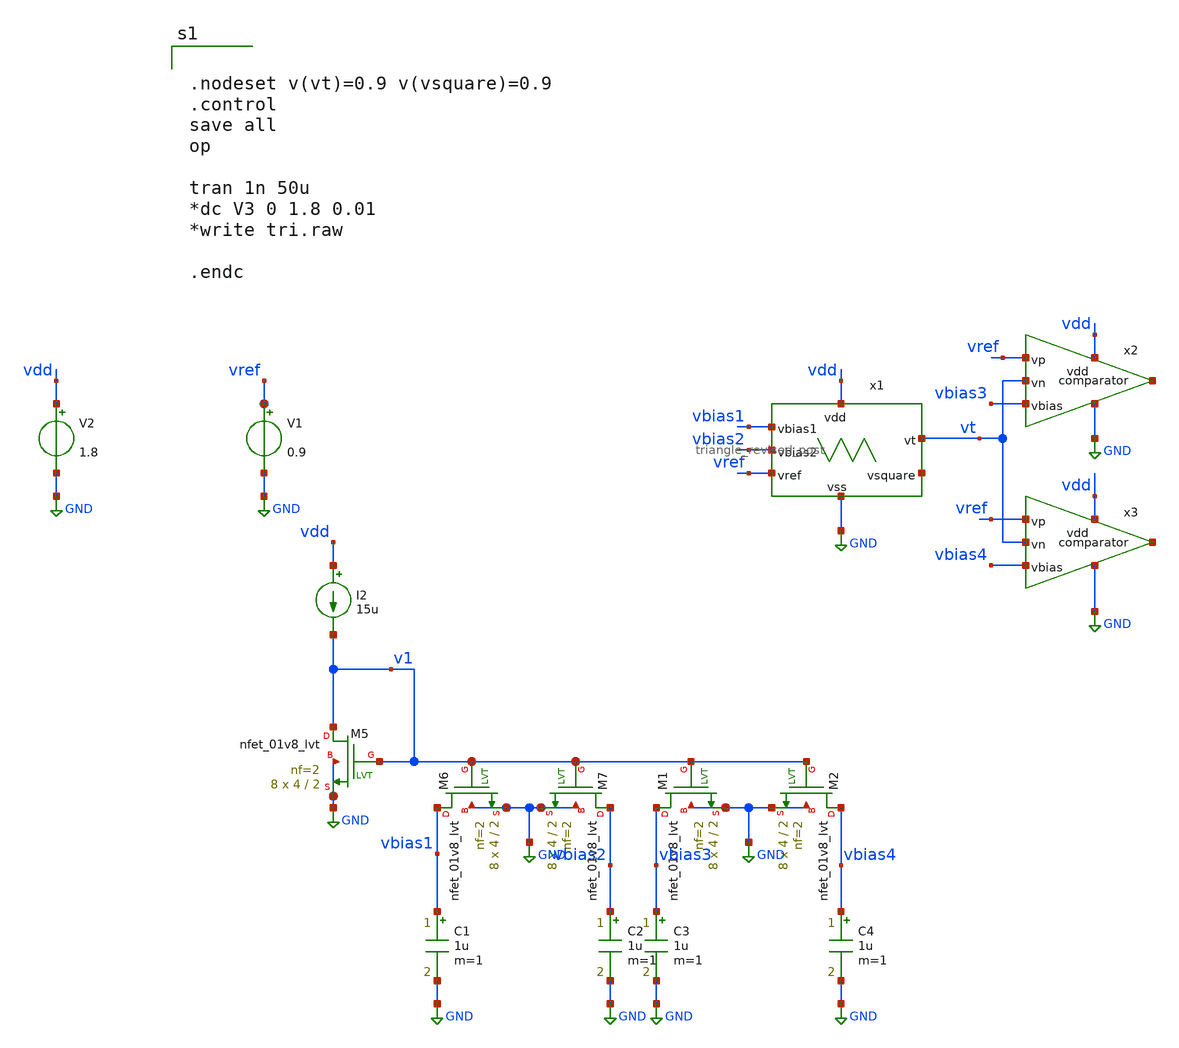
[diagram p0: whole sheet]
** sch_path: xschem/src/triangle/triangle_tb.sch
**.subckt triangle_tb
V1 vref GND 0.9
V2 vdd GND 1.8
I2 vdd v1 15u
XM5 v1 v1 GND GND sky130_fd_pr__nfet_01v8_lvt L=2 W=4 nf=2 ad='int((nf+1)/2) * W/nf * 0.29' as='int((nf+2)/2) * W/nf * 0.29'
+ pd='2*int((nf+1)/2) * (W/nf + 0.29)' ps='2*int((nf+2)/2) * (W/nf + 0.29)' nrd='0.29 / W' nrs='0.29 / W'
+ sa=0 sb=0 sd=0 mult=8 m=8
XM6 vbias1 v1 GND GND sky130_fd_pr__nfet_01v8_lvt L=2 W=4 nf=2 ad='int((nf+1)/2) * W/nf * 0.29' as='int((nf+2)/2) * W/nf * 0.29'
+ pd='2*int((nf+1)/2) * (W/nf + 0.29)' ps='2*int((nf+2)/2) * (W/nf + 0.29)' nrd='0.29 / W' nrs='0.29 / W'
+ sa=0 sb=0 sd=0 mult=8 m=8
XM7 vbias2 v1 GND GND sky130_fd_pr__nfet_01v8_lvt L=2 W=4 nf=2 ad='int((nf+1)/2) * W/nf * 0.29' as='int((nf+2)/2) * W/nf * 0.29'
+ pd='2*int((nf+1)/2) * (W/nf + 0.29)' ps='2*int((nf+2)/2) * (W/nf + 0.29)' nrd='0.29 / W' nrs='0.29 / W'
+ sa=0 sb=0 sd=0 mult=8 m=8
XM1 vbias3 v1 GND GND sky130_fd_pr__nfet_01v8_lvt L=2 W=4 nf=2 ad='int((nf+1)/2) * W/nf * 0.29' as='int((nf+2)/2) * W/nf * 0.29'
+ pd='2*int((nf+1)/2) * (W/nf + 0.29)' ps='2*int((nf+2)/2) * (W/nf + 0.29)' nrd='0.29 / W' nrs='0.29 / W'
+ sa=0 sb=0 sd=0 mult=8 m=8
XM2 vbias4 v1 GND GND sky130_fd_pr__nfet_01v8_lvt L=2 W=4 nf=2 ad='int((nf+1)/2) * W/nf * 0.29' as='int((nf+2)/2) * W/nf * 0.29'
+ pd='2*int((nf+1)/2) * (W/nf + 0.29)' ps='2*int((nf+2)/2) * (W/nf + 0.29)' nrd='0.29 / W' nrs='0.29 / W'
+ sa=0 sb=0 sd=0 mult=8 m=8
C1 vbias1 GND 1u m=1
C2 vbias2 GND 1u m=1
C3 vbias3 GND 1u m=1
C4 vbias4 GND 1u m=1
x2 vdd vref vt vbias3 GND net1 comparator
x3 vdd vref vt vbias4 GND net2 comparator
x1 vdd vbias1 vbias2 vref GND net3 vt triangle_revised_post
**** begin user architecture code

.include /home/eda/pdk/skywater-pdk/libraries/sky130_fd_pr_ngspice/latest/models/corners/tt.spice
.include /home/eda/magic/class_d_audio_amplifier/OTA/OTA_tri_post.spice
.include /home/eda/magic/class_d_audio_amplifier/OTA/OTA_post.spice
.include /home/eda/magic/class_d_audio_amplifier/triang/triangle_post.spice
.include /home/eda/magic/class_d_audio_amplifier/OTA/OTA_int_revised_post.spice
.include /home/eda/magic/class_d_audio_amplifier/OTA/OTA_revised_post.spice
.include /home/eda/magic/class_d_audio_amplifier/OTA/OTA_tri_revised_post.spice
.include /home/eda/magic/class_d_audio_amplifier/triang/triangle_revised_post.spice
* Resistor$::SKYWATER_MODELS/Capacitor
.include $::SKYWATER_MODELS/models/r+c/res_typical__cap_typical.spice
.include $::SKYWATER_MODELS/models/r+c/res_typical__cap_typical__lin.spice
* Special cells
.include $::SKYWATER_MODELS/models/corners/tt/specialized_cells.spice




.nodeset v(vt)=0.9 v(vsquare)=0.9
.control
save all
op

tran 1n 50u
*dc V3 0 1.8 0.01
*write tri.raw

.endc


**** end user architecture code
**.ends

* expanding   symbol:  src/comparator/comparator.sym # of pins=6
** sym_path: xschem/src/comparator/comparator.sym
** sch_path: xschem/src/comparator/comparator.sch
.subckt comparator vdd vp vn vbias vss vout
*.ipin vp
*.ipin vn
*.ipin vbias
*.iopin vss
*.iopin vdd
*.opin vout
XM1 v1 vp vc vc sky130_fd_pr__pfet_01v8_lvt L=1 W=4 nf=1 ad='int((nf+1)/2) * W/nf * 0.29' as='int((nf+2)/2) * W/nf * 0.29'
+ pd='2*int((nf+1)/2) * (W/nf + 0.29)' ps='2*int((nf+2)/2) * (W/nf + 0.29)' nrd='0.29 / W' nrs='0.29 / W'
+ sa=0 sb=0 sd=0 mult=16 m=16
XM2 vf vn vc vc sky130_fd_pr__pfet_01v8_lvt L=1 W=4 nf=1 ad='int((nf+1)/2) * W/nf * 0.29' as='int((nf+2)/2) * W/nf * 0.29'
+ pd='2*int((nf+1)/2) * (W/nf + 0.29)' ps='2*int((nf+2)/2) * (W/nf + 0.29)' nrd='0.29 / W' nrs='0.29 / W'
+ sa=0 sb=0 sd=0 mult=16 m=16
XM3 vc vbias vdd vdd sky130_fd_pr__pfet_01v8_lvt L=1 W=2 nf=2 ad='int((nf+1)/2) * W/nf * 0.29' as='int((nf+2)/2) * W/nf * 0.29'
+ pd='2*int((nf+1)/2) * (W/nf + 0.29)' ps='2*int((nf+2)/2) * (W/nf + 0.29)' nrd='0.29 / W' nrs='0.29 / W'
+ sa=0 sb=0 sd=0 mult=24 m=24
XM4 v1 vf vss vss sky130_fd_pr__nfet_01v8_lvt L=1 W=1 nf=1 ad='int((nf+1)/2) * W/nf * 0.29' as='int((nf+2)/2) * W/nf * 0.29'
+ pd='2*int((nf+1)/2) * (W/nf + 0.29)' ps='2*int((nf+2)/2) * (W/nf + 0.29)' nrd='0.29 / W' nrs='0.29 / W'
+ sa=0 sb=0 sd=0 mult=16 m=16
XM5 vf vf vss vss sky130_fd_pr__nfet_01v8_lvt L=1 W=1 nf=1 ad='int((nf+1)/2) * W/nf * 0.29' as='int((nf+2)/2) * W/nf * 0.29'
+ pd='2*int((nf+1)/2) * (W/nf + 0.29)' ps='2*int((nf+2)/2) * (W/nf + 0.29)' nrd='0.29 / W' nrs='0.29 / W'
+ sa=0 sb=0 sd=0 mult=16 m=16
XM6 vbias vbias vdd vdd sky130_fd_pr__pfet_01v8_lvt L=1 W=2 nf=2 ad='int((nf+1)/2) * W/nf * 0.29' as='int((nf+2)/2) * W/nf * 0.29'
+ pd='2*int((nf+1)/2) * (W/nf + 0.29)' ps='2*int((nf+2)/2) * (W/nf + 0.29)' nrd='0.29 / W' nrs='0.29 / W'
+ sa=0 sb=0 sd=0 mult=24 m=24
XM7 vout vbias vdd vdd sky130_fd_pr__pfet_01v8_lvt L=1 W=2 nf=2 ad='int((nf+1)/2) * W/nf * 0.29' as='int((nf+2)/2) * W/nf * 0.29'
+ pd='2*int((nf+1)/2) * (W/nf + 0.29)' ps='2*int((nf+2)/2) * (W/nf + 0.29)' nrd='0.29 / W' nrs='0.29 / W'
+ sa=0 sb=0 sd=0 mult=48 m=48
XM8 vout v1 vss vss sky130_fd_pr__nfet_01v8_lvt L=1 W=1 nf=1 ad='int((nf+1)/2) * W/nf * 0.29' as='int((nf+2)/2) * W/nf * 0.29'
+ pd='2*int((nf+1)/2) * (W/nf + 0.29)' ps='2*int((nf+2)/2) * (W/nf + 0.29)' nrd='0.29 / W' nrs='0.29 / W'
+ sa=0 sb=0 sd=0 mult=64 m=64
.ends

.GLOBAL GND
.end
